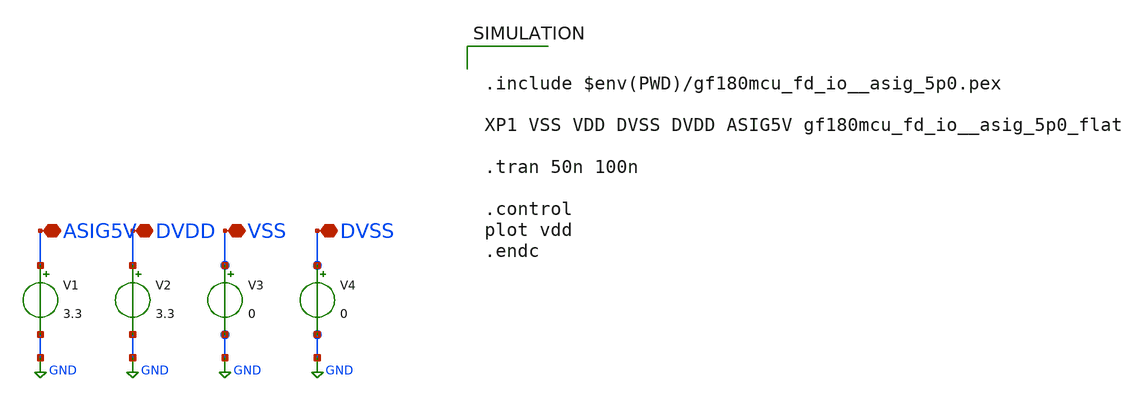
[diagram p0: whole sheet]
** sch_path: extraction/pex/analog.sch

.include $env(PDK_ROOT)/gf180mcuD/libs.tech/ngspice/design.ngspice
.lib $env(PDK_ROOT)/$env(PDK)/libs.tech/ngspice/sm141064.ngspice typical
.lib $env(PDK_ROOT)/$env(PDK)/libs.tech/ngspice/sm141064.ngspice diode_typical
.lib $env(PDK_ROOT)/$env(PDK)/libs.tech/ngspice/sm141064.ngspice res_typical
.lib $env(PDK_ROOT)/$env(PDK)/libs.tech/ngspice/sm141064.ngspice bjt_typical
.lib $env(PDK_ROOT)/$env(PDK)/libs.tech/ngspice/sm141064.ngspice mimcap_typical
.lib $env(PDK_ROOT)/$env(PDK)/libs.tech/ngspice/sm141064.ngspice moscap_typical


.include $env(PWD)/gf180mcu_fd_io__asig_5p0.pex

XP1 VSS VDD DVSS DVDD ASIG5V gf180mcu_fd_io__asig_5p0_flat

.tran 50n 100n

.control
plot vdd
.endc


**.subckt analog ASIG5V DVDD VSS DVSS
*.iopin ASIG5V
*.iopin DVDD
*.iopin VSS
*.iopin DVSS
V1 ASIG5V GND 3.3
V2 DVDD GND 3.3
V3 VSS GND 0
V4 DVSS GND 0
**.ends
.GLOBAL GND
.end
